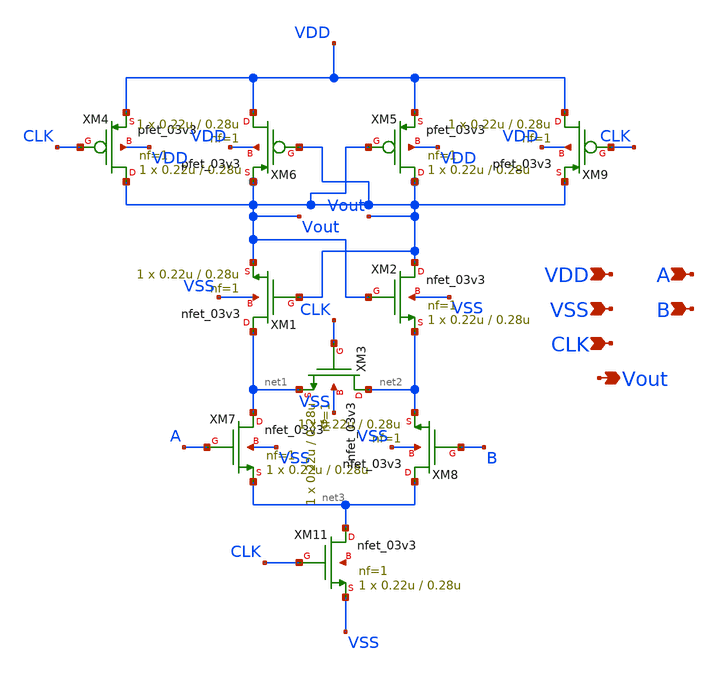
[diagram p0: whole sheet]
** sch_path: strongarm.sch
**.subckt strongarm VDD VSS CLK Vout A B
*.ipin VDD
*.ipin VSS
*.ipin CLK
*.opin Vout
*.ipin A
*.ipin B
XM1 net1 Vout Vout VSS nfet_03v3 L=0.28u W=0.22u nf=1 ad='int((nf+1)/2) * W/nf * 0.18u' as='int((nf+2)/2) * W/nf * 0.18u'
+ pd='2*int((nf+1)/2) * (W/nf + 0.18u)' ps='2*int((nf+2)/2) * (W/nf + 0.18u)' nrd='0.18u / W' nrs='0.18u / W'
+ sa=0 sb=0 sd=0 m=1
XM2 Vout Vout net2 VSS nfet_03v3 L=0.28u W=0.22u nf=1 ad='int((nf+1)/2) * W/nf * 0.18u' as='int((nf+2)/2) * W/nf * 0.18u'
+ pd='2*int((nf+1)/2) * (W/nf + 0.18u)' ps='2*int((nf+2)/2) * (W/nf + 0.18u)' nrd='0.18u / W' nrs='0.18u / W'
+ sa=0 sb=0 sd=0 m=1
XM4 Vout CLK VDD VDD pfet_03v3 L=0.28u W=0.22u nf=1 ad='int((nf+1)/2) * W/nf * 0.18u' as='int((nf+2)/2) * W/nf * 0.18u'
+ pd='2*int((nf+1)/2) * (W/nf + 0.18u)' ps='2*int((nf+2)/2) * (W/nf + 0.18u)' nrd='0.18u / W' nrs='0.18u / W'
+ sa=0 sb=0 sd=0 m=1
XM5 Vout Vout VDD VDD pfet_03v3 L=0.28u W=0.22u nf=1 ad='int((nf+1)/2) * W/nf * 0.18u' as='int((nf+2)/2) * W/nf * 0.18u'
+ pd='2*int((nf+1)/2) * (W/nf + 0.18u)' ps='2*int((nf+2)/2) * (W/nf + 0.18u)' nrd='0.18u / W' nrs='0.18u / W'
+ sa=0 sb=0 sd=0 m=1
XM6 VDD Vout Vout VDD pfet_03v3 L=0.28u W=0.22u nf=1 ad='int((nf+1)/2) * W/nf * 0.18u' as='int((nf+2)/2) * W/nf * 0.18u'
+ pd='2*int((nf+1)/2) * (W/nf + 0.18u)' ps='2*int((nf+2)/2) * (W/nf + 0.18u)' nrd='0.18u / W' nrs='0.18u / W'
+ sa=0 sb=0 sd=0 m=1
XM9 VDD CLK Vout VDD pfet_03v3 L=0.28u W=0.22u nf=1 ad='int((nf+1)/2) * W/nf * 0.18u' as='int((nf+2)/2) * W/nf * 0.18u'
+ pd='2*int((nf+1)/2) * (W/nf + 0.18u)' ps='2*int((nf+2)/2) * (W/nf + 0.18u)' nrd='0.18u / W' nrs='0.18u / W'
+ sa=0 sb=0 sd=0 m=1
XM7 net1 A net3 VSS nfet_03v3 L=0.28u W=0.22u nf=1 ad='int((nf+1)/2) * W/nf * 0.18u' as='int((nf+2)/2) * W/nf * 0.18u'
+ pd='2*int((nf+1)/2) * (W/nf + 0.18u)' ps='2*int((nf+2)/2) * (W/nf + 0.18u)' nrd='0.18u / W' nrs='0.18u / W'
+ sa=0 sb=0 sd=0 m=1
XM8 net3 B net2 VSS nfet_03v3 L=0.28u W=0.22u nf=1 ad='int((nf+1)/2) * W/nf * 0.18u' as='int((nf+2)/2) * W/nf * 0.18u'
+ pd='2*int((nf+1)/2) * (W/nf + 0.18u)' ps='2*int((nf+2)/2) * (W/nf + 0.18u)' nrd='0.18u / W' nrs='0.18u / W'
+ sa=0 sb=0 sd=0 m=1
XM11 net3 CLK VSS net4 nfet_03v3 L=0.28u W=0.22u nf=1 ad='int((nf+1)/2) * W/nf * 0.18u' as='int((nf+2)/2) * W/nf * 0.18u'
+ pd='2*int((nf+1)/2) * (W/nf + 0.18u)' ps='2*int((nf+2)/2) * (W/nf + 0.18u)' nrd='0.18u / W' nrs='0.18u / W'
+ sa=0 sb=0 sd=0 m=1
XM3 net2 CLK net1 VSS nfet_03v3 L=0.28u W=0.22u nf=1 ad='int((nf+1)/2) * W/nf * 0.18u' as='int((nf+2)/2) * W/nf * 0.18u'
+ pd='2*int((nf+1)/2) * (W/nf + 0.18u)' ps='2*int((nf+2)/2) * (W/nf + 0.18u)' nrd='0.18u / W' nrs='0.18u / W'
+ sa=0 sb=0 sd=0 m=1
**.ends
.end
